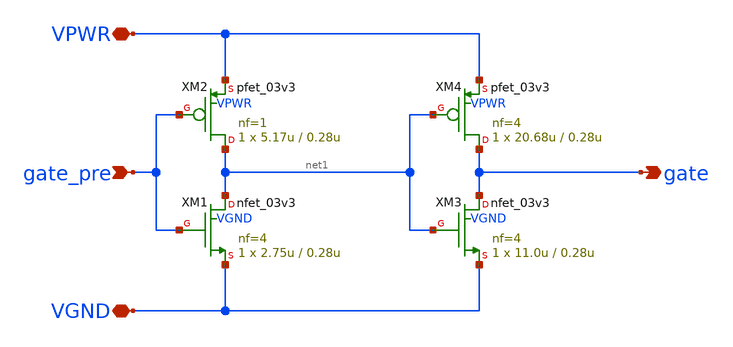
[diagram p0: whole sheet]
** sch_path: pg/gf180mcuD/common/xschem/gate_drv_3v3.sch
**.subckt gate_drv_3v3 VPWR VGND gate_pre gate
*.iopin VPWR
*.iopin VGND
*.ipin gate_pre
*.opin gate
XM1 net1 gate_pre VGND VGND nfet_03v3 L=0.28u W=2.75u nf=4 ad='int((nf+1)/2) * W/nf * 0.18u' as='int((nf+2)/2) * W/nf * 0.18u'
+ pd='2*int((nf+1)/2) * (W/nf + 0.18u)' ps='2*int((nf+2)/2) * (W/nf + 0.18u)' nrd='0.18u / W' nrs='0.18u / W'
+ sa=0 sb=0 sd=0 m=1 par=1
XM2 net1 gate_pre VPWR VPWR pfet_03v3 L=0.28u W=5.17u nf=1 ad='int((nf+1)/2) * W/nf * 0.18u' as='int((nf+2)/2) * W/nf * 0.18u'
+ pd='2*int((nf+1)/2) * (W/nf + 0.18u)' ps='2*int((nf+2)/2) * (W/nf + 0.18u)' nrd='0.18u / W' nrs='0.18u / W'
+ sa=0 sb=0 sd=0 m=1 par=1
XM3 gate net1 VGND VGND nfet_03v3 L=0.28u W=11.0u nf=4 ad='int((nf+1)/2) * W/nf * 0.18u' as='int((nf+2)/2) * W/nf * 0.18u'
+ pd='2*int((nf+1)/2) * (W/nf + 0.18u)' ps='2*int((nf+2)/2) * (W/nf + 0.18u)' nrd='0.18u / W' nrs='0.18u / W'
+ sa=0 sb=0 sd=0 m=1 par=1
XM4 gate net1 VPWR VPWR pfet_03v3 L=0.28u W=20.68u nf=4 ad='int((nf+1)/2) * W/nf * 0.18u' as='int((nf+2)/2) * W/nf * 0.18u'
+ pd='2*int((nf+1)/2) * (W/nf + 0.18u)' ps='2*int((nf+2)/2) * (W/nf + 0.18u)' nrd='0.18u / W' nrs='0.18u / W'
+ sa=0 sb=0 sd=0 m=1 par=1
**.ends
.end
